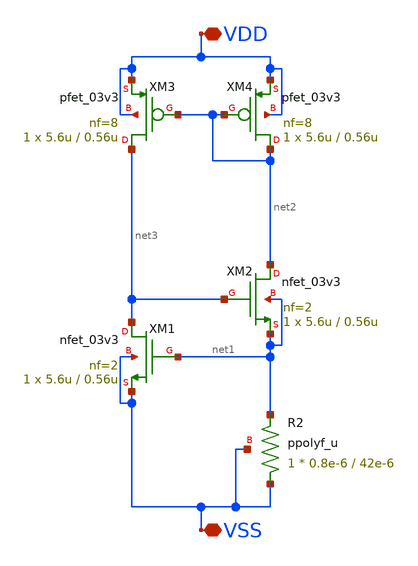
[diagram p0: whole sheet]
** sch_path: cs-vth-ref03v3.sch
**.subckt cs-vth-ref03v3 VSS VDD
*.iopin VSS
*.iopin VDD
XM1 net3 net1 VSS VSS nfet_03v3 L=0.56u W=5.6u nf=2 ad='int((nf+1)/2) * W/nf * 0.18u' as='int((nf+2)/2) * W/nf * 0.18u'
+ pd='2*int((nf+1)/2) * (W/nf + 0.18u)' ps='2*int((nf+2)/2) * (W/nf + 0.18u)' nrd='0.18u / W' nrs='0.18u / W'
+ sa=0 sb=0 sd=0 m=1
XM2 net2 net3 net1 net1 nfet_03v3 L=0.56u W=5.6u nf=2 ad='int((nf+1)/2) * W/nf * 0.18u' as='int((nf+2)/2) * W/nf * 0.18u'
+ pd='2*int((nf+1)/2) * (W/nf + 0.18u)' ps='2*int((nf+2)/2) * (W/nf + 0.18u)' nrd='0.18u / W' nrs='0.18u / W'
+ sa=0 sb=0 sd=0 m=1
XM3 net3 net2 VDD VDD pfet_03v3 L=0.56u W=5.6u nf=8 ad='int((nf+1)/2) * W/nf * 0.18u' as='int((nf+2)/2) * W/nf * 0.18u'
+ pd='2*int((nf+1)/2) * (W/nf + 0.18u)' ps='2*int((nf+2)/2) * (W/nf + 0.18u)' nrd='0.18u / W' nrs='0.18u / W'
+ sa=0 sb=0 sd=0 m=1
XM4 net2 net2 VDD VDD pfet_03v3 L=0.56u W=5.6u nf=8 ad='int((nf+1)/2) * W/nf * 0.18u' as='int((nf+2)/2) * W/nf * 0.18u'
+ pd='2*int((nf+1)/2) * (W/nf + 0.18u)' ps='2*int((nf+2)/2) * (W/nf + 0.18u)' nrd='0.18u / W' nrs='0.18u / W'
+ sa=0 sb=0 sd=0 m=1
XR2 VSS net1 VSS ppolyf_u r_width=0.8e-6 r_length=42e-6 m=1
**.ends
.end
